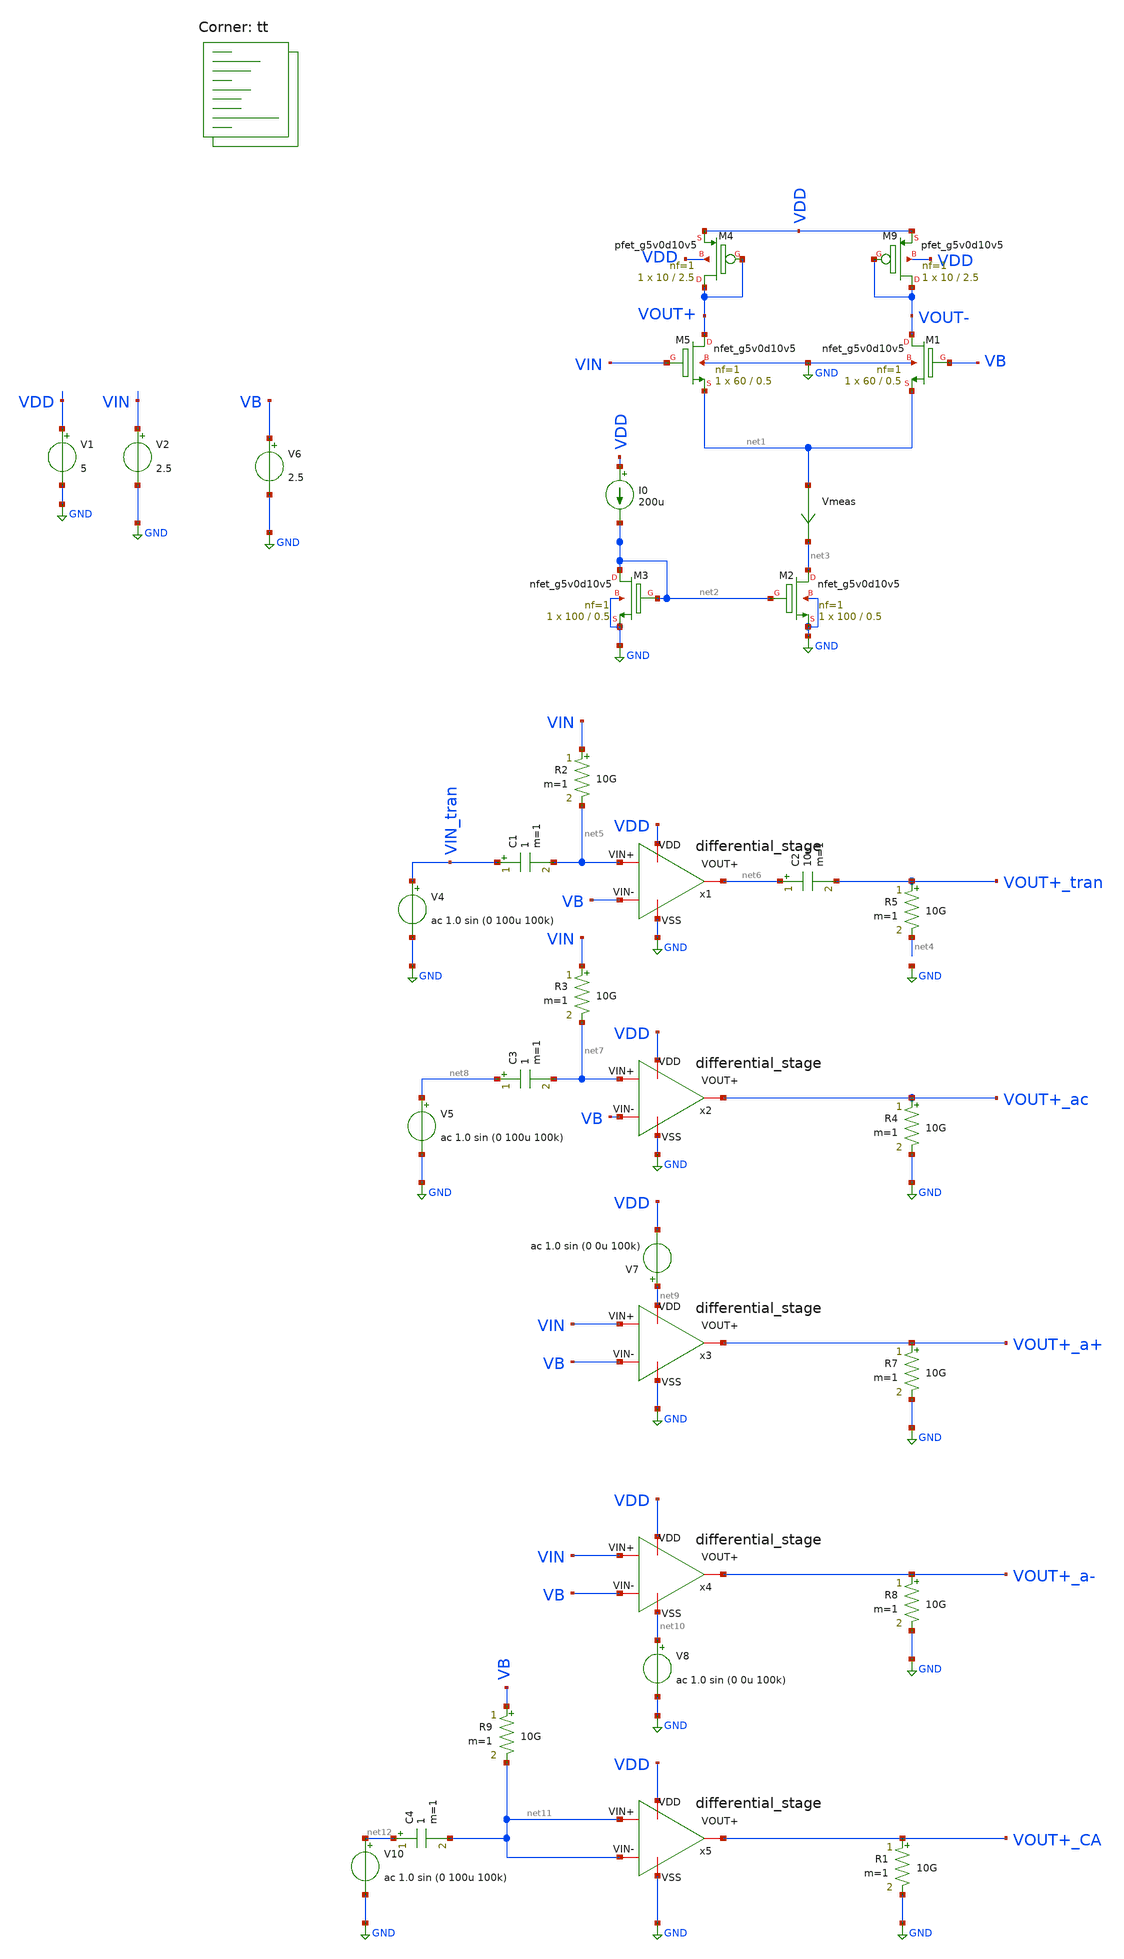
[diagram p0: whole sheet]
** sch_path: amplifiers/differencial_stage_amps/basic_stages/basic_NMOS_diode_stage/diferential_stage.sch
**.subckt diferential_stage
XM5 VOUT+ VIN net1 GND sky130_fd_pr__nfet_g5v0d10v5 L=0.5 W=60 nf=1 ad='int((1 + 1)/2) * 60 / 1 * 0.29'
+ as='int((1 + 2)/2) * 60 / 1 * 0.29' pd='2*int((1 + 1)/2) * (60 / 1 + 0.29)' ps='2*int((1 + 2)/2) * (60 / 1 + 0.29)'
+ nrd='0.29 / 60 ' nrs='0.29 / 60 ' sa=0 sb=0 sd=0 mult=1 m=1
XM1 VOUT- VB net1 GND sky130_fd_pr__nfet_g5v0d10v5 L=0.5 W=60 nf=1 ad='int((1 + 1)/2) * 60 / 1 * 0.29'
+ as='int((1 + 2)/2) * 60 / 1 * 0.29' pd='2*int((1 + 1)/2) * (60 / 1 + 0.29)' ps='2*int((1 + 2)/2) * (60 / 1 + 0.29)'
+ nrd='0.29 / 60 ' nrs='0.29 / 60 ' sa=0 sb=0 sd=0 mult=1 m=1
V1 VDD GND 5
V2 VIN GND 2.5
V6 VB GND 2.5
XM2 net3 net2 GND GND sky130_fd_pr__nfet_g5v0d10v5 L=0.5 W=100 nf=1 ad='int((1 + 1)/2) * 100 / 1 * 0.29'
+ as='int((1 + 2)/2) * 100 / 1 * 0.29' pd='2*int((1 + 1)/2) * (100 / 1 + 0.29)' ps='2*int((1 + 2)/2) * (100 / 1 + 0.29)'
+ nrd='0.29 / 100 ' nrs='0.29 / 100 ' sa=0 sb=0 sd=0 mult=1 m=1
Vmeas net1 net3 0
.save i(vmeas)
R5 VOUT+_tran net4 10G m=1
R2 VIN net5 10G m=1
V4 VIN_tran GND ac 1.0 sin (0 100u 100k)
C2 net6 VOUT+_tran 10u m=1
C1 VIN_tran net5 1 m=1
R3 VIN net7 10G m=1
C3 net8 net7 1 m=1
V5 net8 GND ac 1.0 sin (0 100u 100k)
R4 VOUT+_ac GND 10G m=1
V7 net9 VDD ac 1.0 sin (0 0u 100k)
R7 VOUT+_a+ GND 10G m=1
V8 net10 GND ac 1.0 sin (0 0u 100k)
R8 VOUT+_a- GND 10G m=1
R9 VB net11 10G m=1
C4 net12 net11 1 m=1
V10 net12 GND ac 1.0 sin (0 100u 100k)
XM3 net2 net2 GND GND sky130_fd_pr__nfet_g5v0d10v5 L=0.5 W=100 nf=1 ad='int((1 + 1)/2) * 100 / 1 * 0.29'
+ as='int((1 + 2)/2) * 100 / 1 * 0.29' pd='2*int((1 + 1)/2) * (100 / 1 + 0.29)' ps='2*int((1 + 2)/2) * (100 / 1 + 0.29)'
+ nrd='0.29 / 100 ' nrs='0.29 / 100 ' sa=0 sb=0 sd=0 mult=1 m=1
I0 VDD net2 200u
x1 VDD GND net5 VB net6 differential_stage
x2 VDD GND net7 VB VOUT+_ac differential_stage
x3 net9 GND VIN VB VOUT+_a+ differential_stage
x4 VDD net10 VIN VB VOUT+_a- differential_stage
x5 VDD GND net11 net11 VOUT+_CA differential_stage
XM9 VOUT- VOUT- VDD VDD sky130_fd_pr__pfet_g5v0d10v5 L=2.5 W=10 nf=1 ad='int((1 + 1)/2) * 10 / 1 * 0.29'
+ as='int((1 + 2)/2) * 10 / 1 * 0.29' pd='2*int((1 + 1)/2) * (10 / 1 + 0.29)' ps='2*int((1 + 2)/2) * (10 / 1 + 0.29)'
+ nrd='0.29 / 10 ' nrs='0.29 / 10 ' sa=0 sb=0 sd=0 mult=1 m=1
XM4 VOUT+ VOUT+ VDD VDD sky130_fd_pr__pfet_g5v0d10v5 L=2.5 W=10 nf=1 ad='int((1 + 1)/2) * 10 / 1 * 0.29'
+ as='int((1 + 2)/2) * 10 / 1 * 0.29' pd='2*int((1 + 1)/2) * (10 / 1 + 0.29)' ps='2*int((1 + 2)/2) * (10 / 1 + 0.29)'
+ nrd='0.29 / 10 ' nrs='0.29 / 10 ' sa=0 sb=0 sd=0 mult=1 m=1
R1 VOUT+_CA GND 10G m=1
**** begin user architecture code

**************************************************************
**************************************************************
**************************************************************
**************************************************************
**************************************************************
*LIBs*********************************************************
**************************************************************
**************************************************************
**************************************************************
**************************************************************
**************************************************************
*.lib $::SKYWATER_MODELS/sky130.lib.spice tt
* chose the corners in the corner file
* tt_mm for mismatch
* ss ff sf fs standart corners
* ll hh lh hl capacitor and resistors corners
* mc for total process variation including corners
**************************************************************
**************************************************************
**************************************************************
**************************************************************
**************************************************************
*Corners/montecarlo options***********************************
**************************************************************
**************************************************************
**************************************************************
**************************************************************
**************************************************************
.TEMP 27
**************************************************************
**************************************************************
**************************************************************
**************************************************************
*SIMULATION and Plots*****************************************
**************************************************************
**************************************************************
**************************************************************
**************************************************************
.control
save all
dc V2 0 5 0.01
*dc simulation
plot v(VOUT-) v(VIN) deriv(v(VOUT-)) v(VOUT+) deriv(v(VOUT+))
*ploting VIN VOUT and the voltage gain
plot i(Vmeas)
*ploting the current for curiosity
tran 0.5ns 20u
*transient simulation
plot (v(VOUT+_tran)) v(VIN_tran)
*simple plot to exemplify the gain
fft v(VOUT+_tran) v(VIN_tran)
*fast fourier transfor
plot mag(v(VOUT+_tran)) mag(v(VIN_tran))
ac dec 20 1 1000G
*simple ac simulation
plot db(v(VOUT+_ac))
plot db(v(VOUT+_a+))
plot db(v(VOUT+_a-))
plot db(v(VOUT+_CA))
plot db((v(VOUT+_ac))/(v(VOUT+_CA)))
plot db((v(VOUT+_ac))/(v(VOUT+_a+)))
plot db((v(VOUT+_ac))/(v(VOUT+_a-)))
.endc

.lib $::SKYWATER_MODELS/sky130.lib.spice tt
**** end user architecture code
**.ends
.GLOBAL GND
.end
